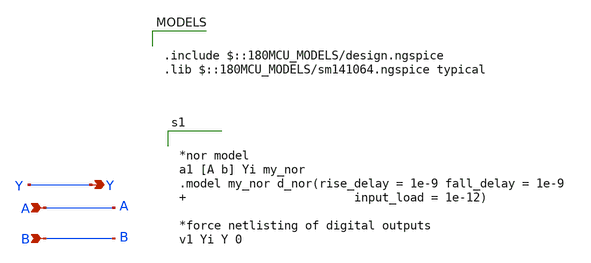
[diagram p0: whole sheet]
** sch_path: XSCHEM Files/nor.sch
**.subckt nor A Y B
*.ipin A
*.opin Y
*.ipin B
**** begin user architecture code


*nor model
a1 [A b] Yi my_nor
.model my_nor d_nor(rise_delay = 1e-9 fall_delay = 1e-9                         input_load = 1e-12)

*force netlisting of digital outputs
v1 Yi Y 0



.include $::180MCU_MODELS/design.ngspice
.lib $::180MCU_MODELS/sm141064.ngspice typical

**** end user architecture code
**.ends
.end
